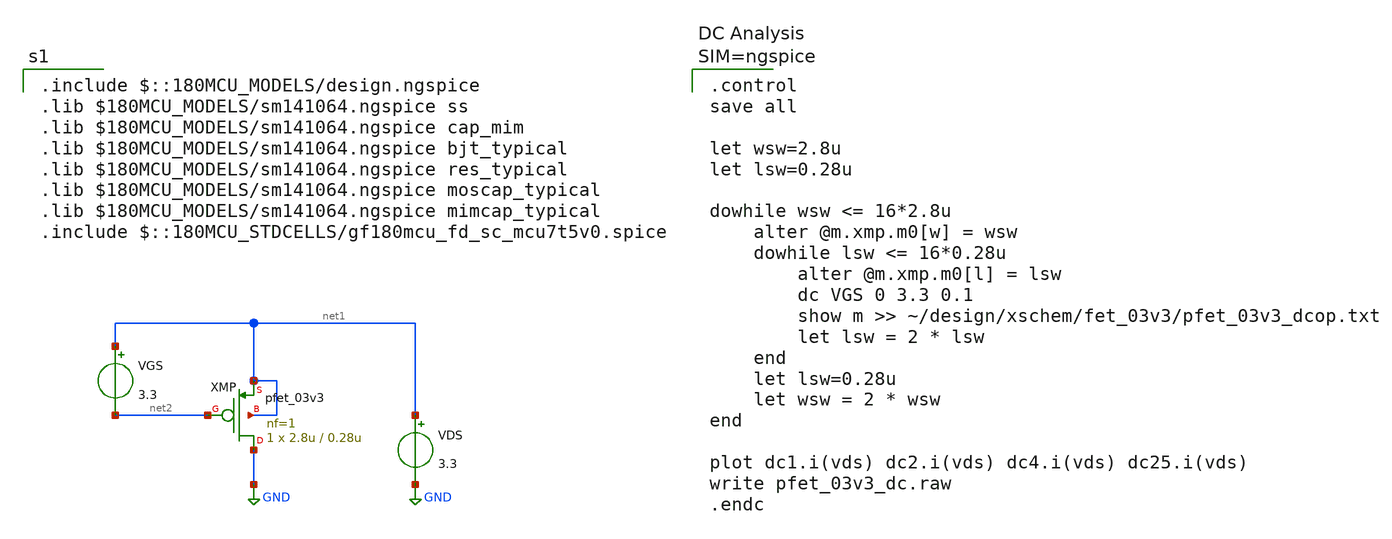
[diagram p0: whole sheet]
** sch_path: DP/fet_03v3/pfet_03v3_dc_oppoint_sweep.sch
**.subckt pfet_03v3_dc_oppoint_sweep
XMP GND net2 net1 net1 pfet_03v3 L=0.28u W=2.8u nf=1 ad='int((nf+1)/2) * W/nf * 0.18u' as='int((nf+2)/2) * W/nf * 0.18u'
+ pd='2*int((nf+1)/2) * (W/nf + 0.18u)' ps='2*int((nf+2)/2) * (W/nf + 0.18u)' nrd='0.18u / W' nrs='0.18u / W'
+ sa=0 sb=0 sd=0 m=1
VGS net1 net2 3.3
VDS net1 GND 3.3
**** begin user architecture code


.control
save all

let wsw=2.8u
let lsw=0.28u

dowhile wsw <= 16*2.8u
	alter @m.xmp.m0[w] = wsw
	dowhile lsw <= 16*0.28u
		alter @m.xmp.m0[l] = lsw
		dc VGS 0 3.3 0.1
		show m >> ~/design/xschem/fet_03v3/pfet_03v3_dcop.txt
		let lsw = 2 * lsw
	end
	let lsw=0.28u
	let wsw = 2 * wsw
end

plot dc1.i(vds) dc2.i(vds) dc4.i(vds) dc25.i(vds)
write pfet_03v3_dc.raw
.endc



 .include $::180MCU_MODELS/design.ngspice
.lib $180MCU_MODELS/sm141064.ngspice ss
.lib $180MCU_MODELS/sm141064.ngspice cap_mim
.lib $180MCU_MODELS/sm141064.ngspice bjt_typical
.lib $180MCU_MODELS/sm141064.ngspice res_typical
.lib $180MCU_MODELS/sm141064.ngspice moscap_typical
.lib $180MCU_MODELS/sm141064.ngspice mimcap_typical
.include $::180MCU_STDCELLS/gf180mcu_fd_sc_mcu7t5v0.spice
**** end user architecture code
**.ends
.GLOBAL GND
.end
